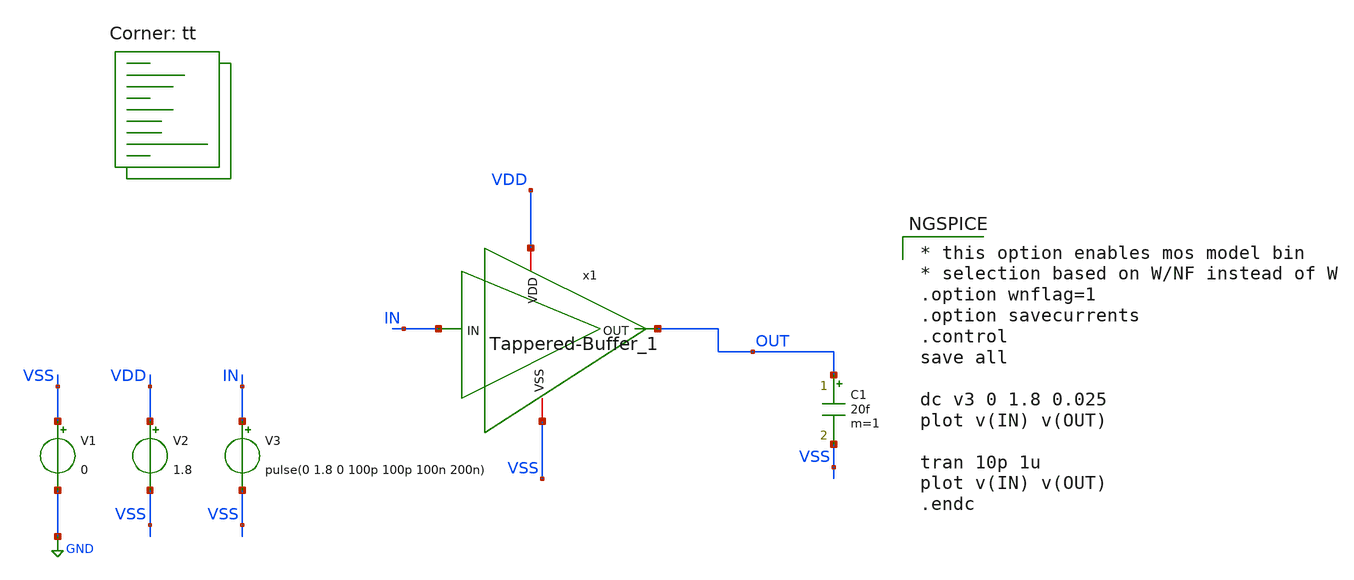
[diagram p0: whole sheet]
** sch_path: Xschem/PLL_TOP_Schematics/inv_tb.sch
**.subckt inv_tb
V1 VSS GND 0
V2 VDD VSS 1.8
V3 IN VSS pulse(0 1.8 0 100p 100p 100n 200n)
C1 OUT VSS 20f m=1
x1 VSS VDD OUT IN Tappered-Buffer_1
**** begin user architecture code

* this option enables mos model bin
* selection based on W/NF instead of W
.option wnflag=1
.option savecurrents
.control
save all

dc v3 0 1.8 0.025
plot v(IN) v(OUT)

tran 10p 1u
plot v(IN) v(OUT)
.endc


.lib $::SKYWATER_MODELS/sky130.lib.spice tt
**** end user architecture code
**.ends

* expanding   symbol:  Tappered-Buffer_1.sym # of pins=4
** sym_path: Xschem/PLL_TOP_Schematics/Tappered-Buffer_1.sym
** sch_path: Xschem/PLL_TOP_Schematics/Tappered-Buffer_1.sch
.subckt Tappered-Buffer_1 VSS VDD OUT IN
*.iopin VDD
*.iopin VSS
*.ipin IN
*.opin OUT
XM1 net1 IN VDD VDD sky130_fd_pr__pfet_01v8 L=0.2 W=4 nf=1 ad='int((nf+1)/2) * W/nf * 0.29' as='int((nf+2)/2) * W/nf * 0.29'
+ pd='2*int((nf+1)/2) * (W/nf + 0.29)' ps='2*int((nf+2)/2) * (W/nf + 0.29)' nrd='0.29 / W' nrs='0.29 / W'
+ sa=0 sb=0 sd=0 mult=2 m=2
XM2 net2 net1 VDD VDD sky130_fd_pr__pfet_01v8 L=0.2 W=8 nf=1 ad='int((nf+1)/2) * W/nf * 0.29' as='int((nf+2)/2) * W/nf * 0.29'
+ pd='2*int((nf+1)/2) * (W/nf + 0.29)' ps='2*int((nf+2)/2) * (W/nf + 0.29)' nrd='0.29 / W' nrs='0.29 / W'
+ sa=0 sb=0 sd=0 mult=2 m=2
XM3 net3 net2 VDD VDD sky130_fd_pr__pfet_01v8 L=0.2 W=16 nf=1 ad='int((nf+1)/2) * W/nf * 0.29' as='int((nf+2)/2) * W/nf * 0.29'
+ pd='2*int((nf+1)/2) * (W/nf + 0.29)' ps='2*int((nf+2)/2) * (W/nf + 0.29)' nrd='0.29 / W' nrs='0.29 / W'
+ sa=0 sb=0 sd=0 mult=2 m=2
XM5 net1 IN VSS VSS sky130_fd_pr__nfet_01v8 L=0.2 W=2 nf=1 ad='int((nf+1)/2) * W/nf * 0.29' as='int((nf+2)/2) * W/nf * 0.29'
+ pd='2*int((nf+1)/2) * (W/nf + 0.29)' ps='2*int((nf+2)/2) * (W/nf + 0.29)' nrd='0.29 / W' nrs='0.29 / W'
+ sa=0 sb=0 sd=0 mult=2 m=2
XM6 net2 net1 VSS VSS sky130_fd_pr__nfet_01v8 L=0.2 W=4 nf=1 ad='int((nf+1)/2) * W/nf * 0.29' as='int((nf+2)/2) * W/nf * 0.29'
+ pd='2*int((nf+1)/2) * (W/nf + 0.29)' ps='2*int((nf+2)/2) * (W/nf + 0.29)' nrd='0.29 / W' nrs='0.29 / W'
+ sa=0 sb=0 sd=0 mult=2 m=2
XM7 net3 net2 VSS VSS sky130_fd_pr__nfet_01v8 L=0.2 W=8 nf=1 ad='int((nf+1)/2) * W/nf * 0.29' as='int((nf+2)/2) * W/nf * 0.29'
+ pd='2*int((nf+1)/2) * (W/nf + 0.29)' ps='2*int((nf+2)/2) * (W/nf + 0.29)' nrd='0.29 / W' nrs='0.29 / W'
+ sa=0 sb=0 sd=0 mult=2 m=2
XM4 OUT net3 VDD VDD sky130_fd_pr__pfet_01v8 L=0.2 W=32 nf=1 ad='int((nf+1)/2) * W/nf * 0.29' as='int((nf+2)/2) * W/nf * 0.29'
+ pd='2*int((nf+1)/2) * (W/nf + 0.29)' ps='2*int((nf+2)/2) * (W/nf + 0.29)' nrd='0.29 / W' nrs='0.29 / W'
+ sa=0 sb=0 sd=0 mult=2 m=2
XM8 OUT net3 VSS VSS sky130_fd_pr__nfet_01v8 L=0.2 W=16 nf=1 ad='int((nf+1)/2) * W/nf * 0.29' as='int((nf+2)/2) * W/nf * 0.29'
+ pd='2*int((nf+1)/2) * (W/nf + 0.29)' ps='2*int((nf+2)/2) * (W/nf + 0.29)' nrd='0.29 / W' nrs='0.29 / W'
+ sa=0 sb=0 sd=0 mult=2 m=2
.ends

.GLOBAL GND
.end
